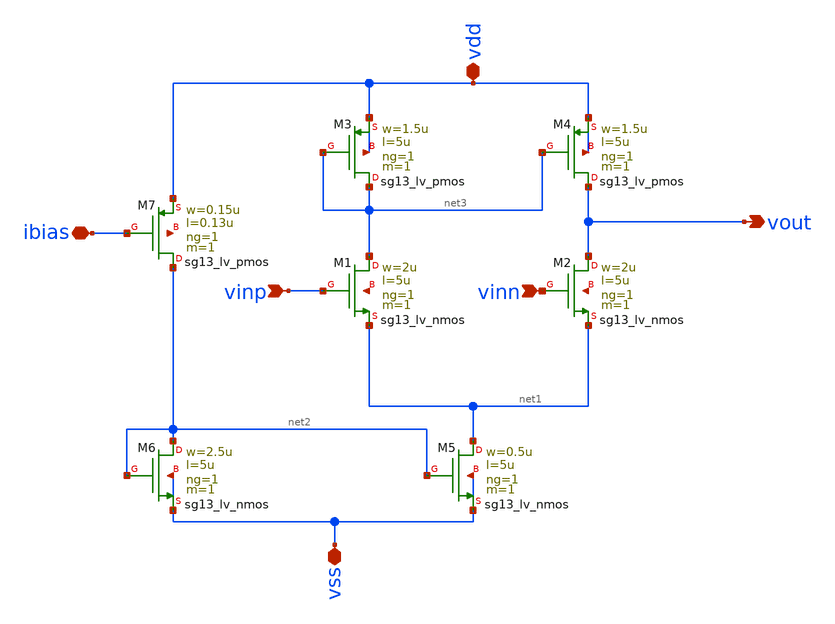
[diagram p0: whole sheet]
** sch_path: 004_Real_Circuits/5T-OTA.sch
**.subckt 5T-OTA vinp vdd vss vout vinn ibias
*.ipin vinp
*.iopin vdd
*.iopin vss
*.opin vout
*.ipin vinn
*.iopin ibias
XM1 net3 vinp net1 net4 sg13_lv_nmos w=2u l=5u ng=1 m=1 mm_ok=1
XM5 net1 net2 vss vss sg13_lv_nmos w=0.5u l=5u ng=1 m=1 mm_ok=1
XM2 vout vinn net1 net5 sg13_lv_nmos w=2u l=5u ng=1 m=1 mm_ok=1
XM6 net2 net2 vss vss sg13_lv_nmos w=2.5u l=5u ng=1 m=1 mm_ok=1
XM3 net3 net3 vdd vdd sg13_lv_pmos w=1.5u l=5u ng=1 m=1 mm_ok=1
XM4 vout net3 vdd vdd sg13_lv_pmos w=1.5u l=5u ng=1 m=1 mm_ok=1
XM7 net2 ibias vdd net6 sg13_lv_pmos w=0.15u l=0.13u ng=1 m=1 mm_ok=1
**.ends
.end
